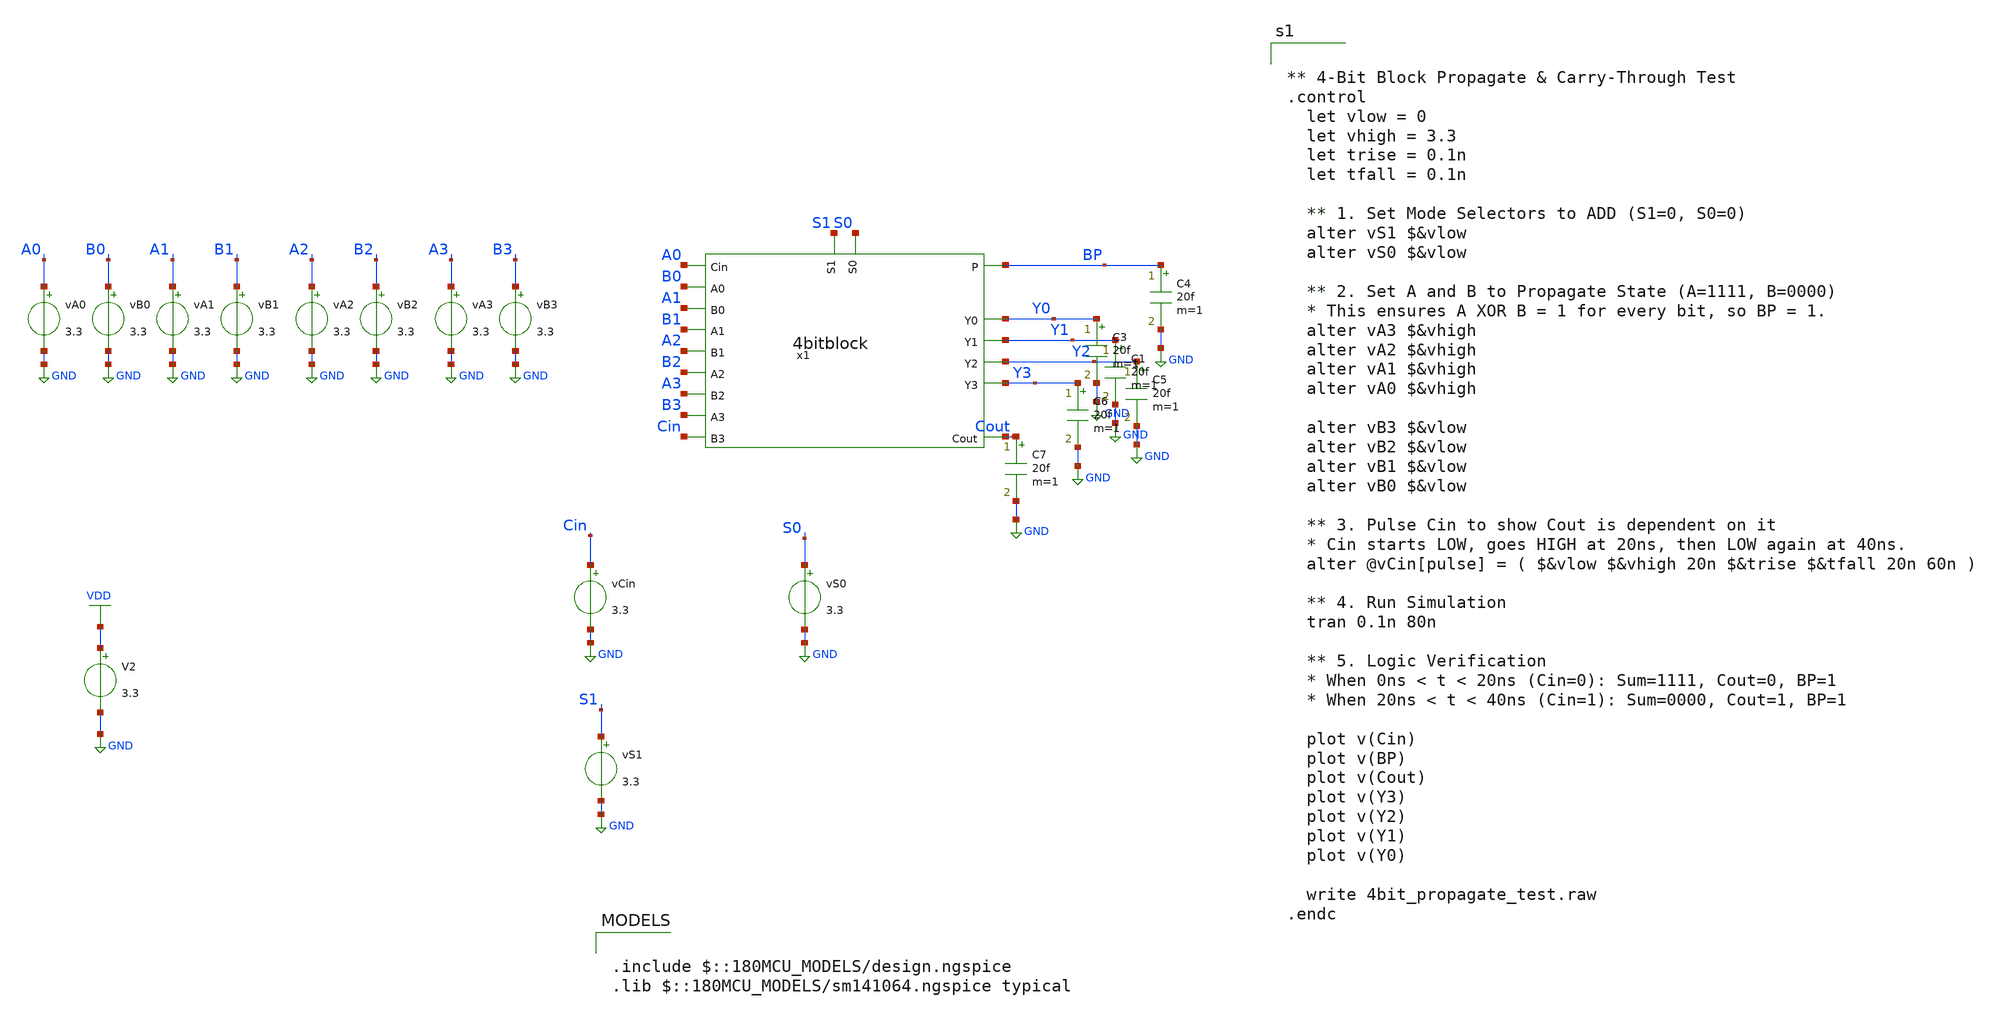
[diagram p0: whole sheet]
** sch_path: tbs/4bit_adding_carrying.sch
**.subckt 4bit_adding_carrying
vA0 A0 GND 3.3
vCin Cin GND 3.3
vS0 S0 GND 3.3
vB0 B0 GND 3.3
vS1 S1 GND 3.3
V2 VDD GND 3.3
x1 S0 BP S1 A0 Y1 Y0 Y3 Y2 B0 Cout A1 B1 A2 B2 A3 B3 Cin 4bitblock
vA1 A1 GND 3.3
vB1 B1 GND 3.3
vA2 A2 GND 3.3
vB2 B2 GND 3.3
vA3 A3 GND 3.3
vB3 B3 GND 3.3
C4 BP GND 20f m=1
C3 Y0 GND 20f m=1
C1 Y1 GND 20f m=1
C5 Y2 GND 20f m=1
C6 Y3 GND 20f m=1
C7 Cout GND 20f m=1
**** begin user architecture code

.include $::180MCU_MODELS/design.ngspice
.lib $::180MCU_MODELS/sm141064.ngspice typical



** 4-Bit Block Propagate & Carry-Through Test
.control
  let vlow = 0
  let vhigh = 3.3
  let trise = 0.1n
  let tfall = 0.1n

  ** 1. Set Mode Selectors to ADD (S1=0, S0=0)
  alter vS1 $&vlow
  alter vS0 $&vlow

  ** 2. Set A and B to Propagate State (A=1111, B=0000)
  * This ensures A XOR B = 1 for every bit, so BP = 1.
  alter vA3 $&vhigh
  alter vA2 $&vhigh
  alter vA1 $&vhigh
  alter vA0 $&vhigh

  alter vB3 $&vlow
  alter vB2 $&vlow
  alter vB1 $&vlow
  alter vB0 $&vlow

  ** 3. Pulse Cin to show Cout is dependent on it
  * Cin starts LOW, goes HIGH at 20ns, then LOW again at 40ns.
  alter @vCin[pulse] = ( $&vlow $&vhigh 20n $&trise $&tfall 20n 60n )

  ** 4. Run Simulation
  tran 0.1n 80n

  ** 5. Logic Verification
  * When 0ns < t < 20ns (Cin=0): Sum=1111, Cout=0, BP=1
  * When 20ns < t < 40ns (Cin=1): Sum=0000, Cout=1, BP=1

  plot v(Cin)
  plot v(BP)
  plot v(Cout)
  plot v(Y3)
  plot v(Y2)
  plot v(Y1)
  plot v(Y0)

  write 4bit_propagate_test.raw
.endc


**** end user architecture code
**.ends
.GLOBAL GND
.GLOBAL VDD
.end
